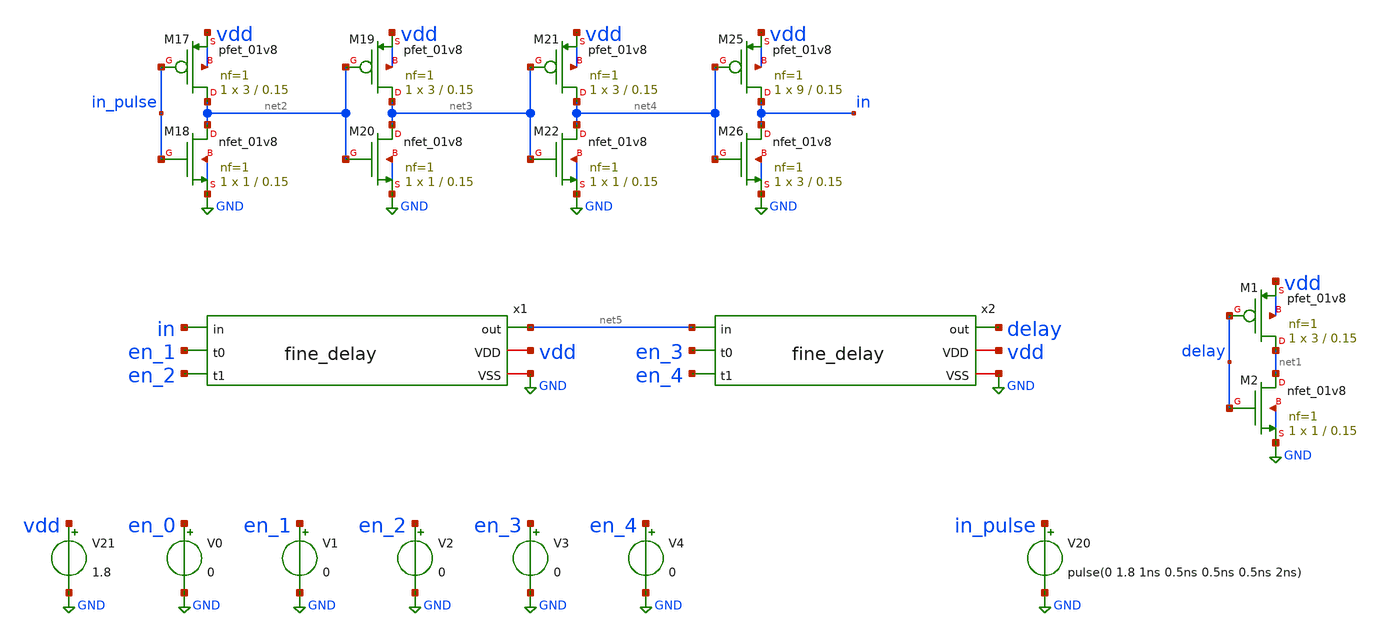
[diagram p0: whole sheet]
** sch_path: xschem/fine_delay_tb.sch
**.subckt fine_delay_tb
V21 vdd GND 1.8
V20 in_pulse GND pulse(0 1.8 1ns 0.5ns 0.5ns 0.5ns 2ns)
XM1 net1 delay vdd vdd sky130_fd_pr__pfet_01v8 L=0.15 W=3 nf=1 ad='int((nf+1)/2) * W/nf * 0.29' as='int((nf+2)/2) * W/nf * 0.29'
+ pd='2*int((nf+1)/2) * (W/nf + 0.29)' ps='2*int((nf+2)/2) * (W/nf + 0.29)' nrd='0.29 / W' nrs='0.29 / W'
+ sa=0 sb=0 sd=0 mult=1 m=1
XM2 net1 delay GND GND sky130_fd_pr__nfet_01v8 L=0.15 W=1 nf=1 ad='int((nf+1)/2) * W/nf * 0.29' as='int((nf+2)/2) * W/nf * 0.29'
+ pd='2*int((nf+1)/2) * (W/nf + 0.29)' ps='2*int((nf+2)/2) * (W/nf + 0.29)' nrd='0.29 / W' nrs='0.29 / W'
+ sa=0 sb=0 sd=0 mult=1 m=1
V0 en_0 GND 0
V1 en_1 GND 0
V2 en_2 GND 0
V3 en_3 GND 0
XM17 net2 in_pulse vdd vdd sky130_fd_pr__pfet_01v8 L=0.15 W=3 nf=1 ad='int((nf+1)/2) * W/nf * 0.29' as='int((nf+2)/2) * W/nf * 0.29'
+ pd='2*int((nf+1)/2) * (W/nf + 0.29)' ps='2*int((nf+2)/2) * (W/nf + 0.29)' nrd='0.29 / W' nrs='0.29 / W'
+ sa=0 sb=0 sd=0 mult=1 m=1
XM18 net2 in_pulse GND GND sky130_fd_pr__nfet_01v8 L=0.15 W=1 nf=1 ad='int((nf+1)/2) * W/nf * 0.29' as='int((nf+2)/2) * W/nf * 0.29'
+ pd='2*int((nf+1)/2) * (W/nf + 0.29)' ps='2*int((nf+2)/2) * (W/nf + 0.29)' nrd='0.29 / W' nrs='0.29 / W'
+ sa=0 sb=0 sd=0 mult=1 m=1
XM19 net3 net2 vdd vdd sky130_fd_pr__pfet_01v8 L=0.15 W=3 nf=1 ad='int((nf+1)/2) * W/nf * 0.29' as='int((nf+2)/2) * W/nf * 0.29'
+ pd='2*int((nf+1)/2) * (W/nf + 0.29)' ps='2*int((nf+2)/2) * (W/nf + 0.29)' nrd='0.29 / W' nrs='0.29 / W'
+ sa=0 sb=0 sd=0 mult=1 m=1
XM20 net3 net2 GND GND sky130_fd_pr__nfet_01v8 L=0.15 W=1 nf=1 ad='int((nf+1)/2) * W/nf * 0.29' as='int((nf+2)/2) * W/nf * 0.29'
+ pd='2*int((nf+1)/2) * (W/nf + 0.29)' ps='2*int((nf+2)/2) * (W/nf + 0.29)' nrd='0.29 / W' nrs='0.29 / W'
+ sa=0 sb=0 sd=0 mult=1 m=1
XM21 net4 net3 vdd vdd sky130_fd_pr__pfet_01v8 L=0.15 W=3 nf=1 ad='int((nf+1)/2) * W/nf * 0.29' as='int((nf+2)/2) * W/nf * 0.29'
+ pd='2*int((nf+1)/2) * (W/nf + 0.29)' ps='2*int((nf+2)/2) * (W/nf + 0.29)' nrd='0.29 / W' nrs='0.29 / W'
+ sa=0 sb=0 sd=0 mult=1 m=1
XM22 net4 net3 GND GND sky130_fd_pr__nfet_01v8 L=0.15 W=1 nf=1 ad='int((nf+1)/2) * W/nf * 0.29' as='int((nf+2)/2) * W/nf * 0.29'
+ pd='2*int((nf+1)/2) * (W/nf + 0.29)' ps='2*int((nf+2)/2) * (W/nf + 0.29)' nrd='0.29 / W' nrs='0.29 / W'
+ sa=0 sb=0 sd=0 mult=1 m=1
XM25 in net4 vdd vdd sky130_fd_pr__pfet_01v8 L=0.15 W=9 nf=1 ad='int((nf+1)/2) * W/nf * 0.29' as='int((nf+2)/2) * W/nf * 0.29'
+ pd='2*int((nf+1)/2) * (W/nf + 0.29)' ps='2*int((nf+2)/2) * (W/nf + 0.29)' nrd='0.29 / W' nrs='0.29 / W'
+ sa=0 sb=0 sd=0 mult=1 m=1
XM26 in net4 GND GND sky130_fd_pr__nfet_01v8 L=0.15 W=3 nf=1 ad='int((nf+1)/2) * W/nf * 0.29' as='int((nf+2)/2) * W/nf * 0.29'
+ pd='2*int((nf+1)/2) * (W/nf + 0.29)' ps='2*int((nf+2)/2) * (W/nf + 0.29)' nrd='0.29 / W' nrs='0.29 / W'
+ sa=0 sb=0 sd=0 mult=1 m=1
x1 in en_1 en_2 net5 vdd GND fine_delay
x2 net5 en_3 en_4 delay vdd GND fine_delay
V4 en_4 GND 0
**** begin user architecture code

** opencircuitdesign pdks install
.lib $::SKYWATER_MODELS/sky130.lib.spice tt





.control
alter V0 0
alter V1 0
alter V2 0
alter V3 0
alter V4 0

foreach i 0 1 2 3 4
alter V$i 1.8

* Run transient analysis
tran 0.0001n 5n

* Save results for this step
save v(in) v(delay)
set wr_vecnames
wrdata fine_delay_tb_$i v(in) v(delay)

end
.endc


**** end user architecture code
**.ends

* expanding   symbol:  fine_delay.sym # of pins=6
** sym_path: xschem/fine_delay.sym
** sch_path: xschem/fine_delay.sch
.subckt fine_delay in t0 t1 out VDD VSS
*.iopin VDD
*.ipin in
*.opin out
*.iopin VSS
*.ipin t0
*.ipin t1
XM1 net1 in VDD VDD sky130_fd_pr__pfet_01v8 L=0.15 W=3 nf=1 ad='int((nf+1)/2) * W/nf * 0.29' as='int((nf+2)/2) * W/nf * 0.29'
+ pd='2*int((nf+1)/2) * (W/nf + 0.29)' ps='2*int((nf+2)/2) * (W/nf + 0.29)' nrd='0.29 / W' nrs='0.29 / W'
+ sa=0 sb=0 sd=0 mult=1 m=1
XM2 net3 in VSS VSS sky130_fd_pr__nfet_01v8 L=0.15 W=1 nf=1 ad='int((nf+1)/2) * W/nf * 0.29' as='int((nf+2)/2) * W/nf * 0.29'
+ pd='2*int((nf+1)/2) * (W/nf + 0.29)' ps='2*int((nf+2)/2) * (W/nf + 0.29)' nrd='0.29 / W' nrs='0.29 / W'
+ sa=0 sb=0 sd=0 mult=1 m=1
XM5 net3 t1 VSS VSS sky130_fd_pr__nfet_01v8 L=0.15 W=2 nf=1 ad='int((nf+1)/2) * W/nf * 0.29' as='int((nf+2)/2) * W/nf * 0.29'
+ pd='2*int((nf+1)/2) * (W/nf + 0.29)' ps='2*int((nf+2)/2) * (W/nf + 0.29)' nrd='0.29 / W' nrs='0.29 / W'
+ sa=0 sb=0 sd=0 mult=1 m=1
XM8 out net1 VDD VDD sky130_fd_pr__pfet_01v8 L=0.15 W=3 nf=1 ad='int((nf+1)/2) * W/nf * 0.29' as='int((nf+2)/2) * W/nf * 0.29'
+ pd='2*int((nf+1)/2) * (W/nf + 0.29)' ps='2*int((nf+2)/2) * (W/nf + 0.29)' nrd='0.29 / W' nrs='0.29 / W'
+ sa=0 sb=0 sd=0 mult=1 m=1
XM9 out net1 VSS VSS sky130_fd_pr__nfet_01v8 L=0.15 W=1 nf=1 ad='int((nf+1)/2) * W/nf * 0.29' as='int((nf+2)/2) * W/nf * 0.29'
+ pd='2*int((nf+1)/2) * (W/nf + 0.29)' ps='2*int((nf+2)/2) * (W/nf + 0.29)' nrd='0.29 / W' nrs='0.29 / W'
+ sa=0 sb=0 sd=0 mult=1 m=1
XM10 net2 in net3 VSS sky130_fd_pr__nfet_01v8 L=0.15 W=1 nf=1 ad='int((nf+1)/2) * W/nf * 0.29' as='int((nf+2)/2) * W/nf * 0.29'
+ pd='2*int((nf+1)/2) * (W/nf + 0.29)' ps='2*int((nf+2)/2) * (W/nf + 0.29)' nrd='0.29 / W' nrs='0.29 / W'
+ sa=0 sb=0 sd=0 mult=1 m=1
XM11 net2 t0 net3 VSS sky130_fd_pr__nfet_01v8 L=0.15 W=2 nf=1 ad='int((nf+1)/2) * W/nf * 0.29' as='int((nf+2)/2) * W/nf * 0.29'
+ pd='2*int((nf+1)/2) * (W/nf + 0.29)' ps='2*int((nf+2)/2) * (W/nf + 0.29)' nrd='0.29 / W' nrs='0.29 / W'
+ sa=0 sb=0 sd=0 mult=1 m=1
XM3 net1 in net2 VSS sky130_fd_pr__nfet_01v8 L=0.15 W=1 nf=1 ad='int((nf+1)/2) * W/nf * 0.29' as='int((nf+2)/2) * W/nf * 0.29'
+ pd='2*int((nf+1)/2) * (W/nf + 0.29)' ps='2*int((nf+2)/2) * (W/nf + 0.29)' nrd='0.29 / W' nrs='0.29 / W'
+ sa=0 sb=0 sd=0 mult=1 m=1
XM4 net1 in net2 VSS sky130_fd_pr__nfet_01v8 L=0.15 W=1 nf=1 ad='int((nf+1)/2) * W/nf * 0.29' as='int((nf+2)/2) * W/nf * 0.29'
+ pd='2*int((nf+1)/2) * (W/nf + 0.29)' ps='2*int((nf+2)/2) * (W/nf + 0.29)' nrd='0.29 / W' nrs='0.29 / W'
+ sa=0 sb=0 sd=0 mult=1 m=1
XM6 net1 in net2 VSS sky130_fd_pr__nfet_01v8 L=0.15 W=1 nf=1 ad='int((nf+1)/2) * W/nf * 0.29' as='int((nf+2)/2) * W/nf * 0.29'
+ pd='2*int((nf+1)/2) * (W/nf + 0.29)' ps='2*int((nf+2)/2) * (W/nf + 0.29)' nrd='0.29 / W' nrs='0.29 / W'
+ sa=0 sb=0 sd=0 mult=1 m=1
.ends

.GLOBAL GND
.end
